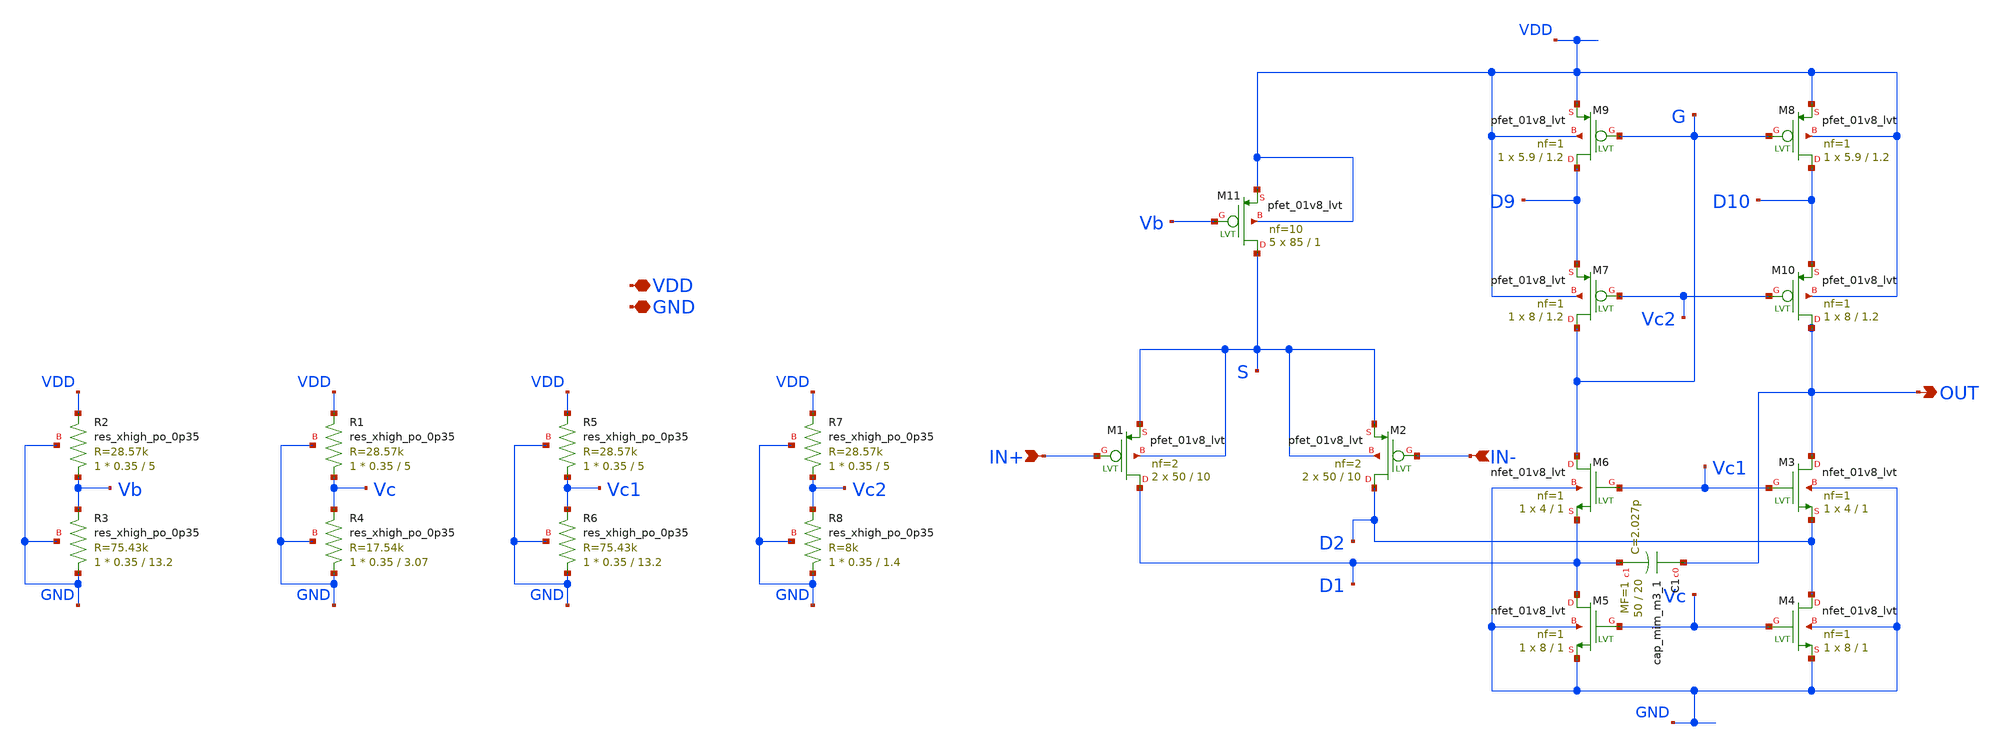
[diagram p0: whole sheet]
** sch_path: xschem/OFC1_1.sch
**.subckt OFC1_1 VDD GND IN+ IN- OUT
*.iopin VDD
*.iopin GND
*.ipin IN+
*.ipin IN-
*.opin OUT
XM11 S Vb VDD VDD sky130_fd_pr__pfet_01v8_lvt L=1 W=85 nf=10 ad='int((nf+1)/2) * W/nf * 0.29' as='int((nf+2)/2) * W/nf * 0.29'
+ pd='2*int((nf+1)/2) * (W/nf + 0.29)' ps='2*int((nf+2)/2) * (W/nf + 0.29)' nrd='0.29 / W' nrs='0.29 / W'
+ sa=0 sb=0 sd=0 mult=5 m=5
XM1 D1 IN+ S S sky130_fd_pr__pfet_01v8_lvt L=10 W=50 nf=2 ad='int((nf+1)/2) * W/nf * 0.29' as='int((nf+2)/2) * W/nf * 0.29'
+ pd='2*int((nf+1)/2) * (W/nf + 0.29)' ps='2*int((nf+2)/2) * (W/nf + 0.29)' nrd='0.29 / W' nrs='0.29 / W'
+ sa=0 sb=0 sd=0 mult=2 m=2
XM2 D2 IN- S S sky130_fd_pr__pfet_01v8_lvt L=10 W=50 nf=2 ad='int((nf+1)/2) * W/nf * 0.29' as='int((nf+2)/2) * W/nf * 0.29'
+ pd='2*int((nf+1)/2) * (W/nf + 0.29)' ps='2*int((nf+2)/2) * (W/nf + 0.29)' nrd='0.29 / W' nrs='0.29 / W'
+ sa=0 sb=0 sd=0 mult=2 m=2
XM3 OUT Vc1 D2 GND sky130_fd_pr__nfet_01v8_lvt L=1 W=4 nf=1 ad='int((nf+1)/2) * W/nf * 0.29' as='int((nf+2)/2) * W/nf * 0.29'
+ pd='2*int((nf+1)/2) * (W/nf + 0.29)' ps='2*int((nf+2)/2) * (W/nf + 0.29)' nrd='0.29 / W' nrs='0.29 / W'
+ sa=0 sb=0 sd=0 mult=1 m=1
XM4 D2 Vc GND GND sky130_fd_pr__nfet_01v8_lvt L=1 W=8 nf=1 ad='int((nf+1)/2) * W/nf * 0.29' as='int((nf+2)/2) * W/nf * 0.29'
+ pd='2*int((nf+1)/2) * (W/nf + 0.29)' ps='2*int((nf+2)/2) * (W/nf + 0.29)' nrd='0.29 / W' nrs='0.29 / W'
+ sa=0 sb=0 sd=0 mult=1 m=1
XM5 D1 Vc GND GND sky130_fd_pr__nfet_01v8_lvt L=1 W=8 nf=1 ad='int((nf+1)/2) * W/nf * 0.29' as='int((nf+2)/2) * W/nf * 0.29'
+ pd='2*int((nf+1)/2) * (W/nf + 0.29)' ps='2*int((nf+2)/2) * (W/nf + 0.29)' nrd='0.29 / W' nrs='0.29 / W'
+ sa=0 sb=0 sd=0 mult=1 m=1
XM6 G Vc1 D1 GND sky130_fd_pr__nfet_01v8_lvt L=1 W=4 nf=1 ad='int((nf+1)/2) * W/nf * 0.29' as='int((nf+2)/2) * W/nf * 0.29'
+ pd='2*int((nf+1)/2) * (W/nf + 0.29)' ps='2*int((nf+2)/2) * (W/nf + 0.29)' nrd='0.29 / W' nrs='0.29 / W'
+ sa=0 sb=0 sd=0 mult=1 m=1
XR2 Vb VDD GND sky130_fd_pr__res_xhigh_po_0p35 L=5 mult=1 m=1
XR3 GND Vb GND sky130_fd_pr__res_xhigh_po_0p35 L=13.2 mult=1 m=1
XR1 Vc VDD GND sky130_fd_pr__res_xhigh_po_0p35 L=5 mult=1 m=1
XR4 GND Vc GND sky130_fd_pr__res_xhigh_po_0p35 L=3.07 mult=1 m=1
XR5 Vc1 VDD GND sky130_fd_pr__res_xhigh_po_0p35 L=5 mult=1 m=1
XR6 GND Vc1 GND sky130_fd_pr__res_xhigh_po_0p35 L=13.2 mult=1 m=1
XR7 Vc2 VDD GND sky130_fd_pr__res_xhigh_po_0p35 L=5 mult=1 m=1
XR8 GND Vc2 GND sky130_fd_pr__res_xhigh_po_0p35 L=1.4 mult=1 m=1
XM7 G Vc2 D9 VDD sky130_fd_pr__pfet_01v8_lvt L=1.2 W=8 nf=1 ad='int((nf+1)/2) * W/nf * 0.29' as='int((nf+2)/2) * W/nf * 0.29'
+ pd='2*int((nf+1)/2) * (W/nf + 0.29)' ps='2*int((nf+2)/2) * (W/nf + 0.29)' nrd='0.29 / W' nrs='0.29 / W'
+ sa=0 sb=0 sd=0 mult=1 m=1
XM9 D9 G VDD VDD sky130_fd_pr__pfet_01v8_lvt L=1.2 W=5.9 nf=1 ad='int((nf+1)/2) * W/nf * 0.29' as='int((nf+2)/2) * W/nf * 0.29'
+ pd='2*int((nf+1)/2) * (W/nf + 0.29)' ps='2*int((nf+2)/2) * (W/nf + 0.29)' nrd='0.29 / W' nrs='0.29 / W'
+ sa=0 sb=0 sd=0 mult=1 m=1
XM8 D10 G VDD VDD sky130_fd_pr__pfet_01v8_lvt L=1.2 W=5.9 nf=1 ad='int((nf+1)/2) * W/nf * 0.29' as='int((nf+2)/2) * W/nf * 0.29'
+ pd='2*int((nf+1)/2) * (W/nf + 0.29)' ps='2*int((nf+2)/2) * (W/nf + 0.29)' nrd='0.29 / W' nrs='0.29 / W'
+ sa=0 sb=0 sd=0 mult=1 m=1
XM10 OUT Vc2 D10 VDD sky130_fd_pr__pfet_01v8_lvt L=1.2 W=8 nf=1 ad='int((nf+1)/2) * W/nf * 0.29' as='int((nf+2)/2) * W/nf * 0.29'
+ pd='2*int((nf+1)/2) * (W/nf + 0.29)' ps='2*int((nf+2)/2) * (W/nf + 0.29)' nrd='0.29 / W' nrs='0.29 / W'
+ sa=0 sb=0 sd=0 mult=1 m=1
XC1 OUT D1 sky130_fd_pr__cap_mim_m3_1 W=50 L=20 MF=1 m=1
**.ends
.end
